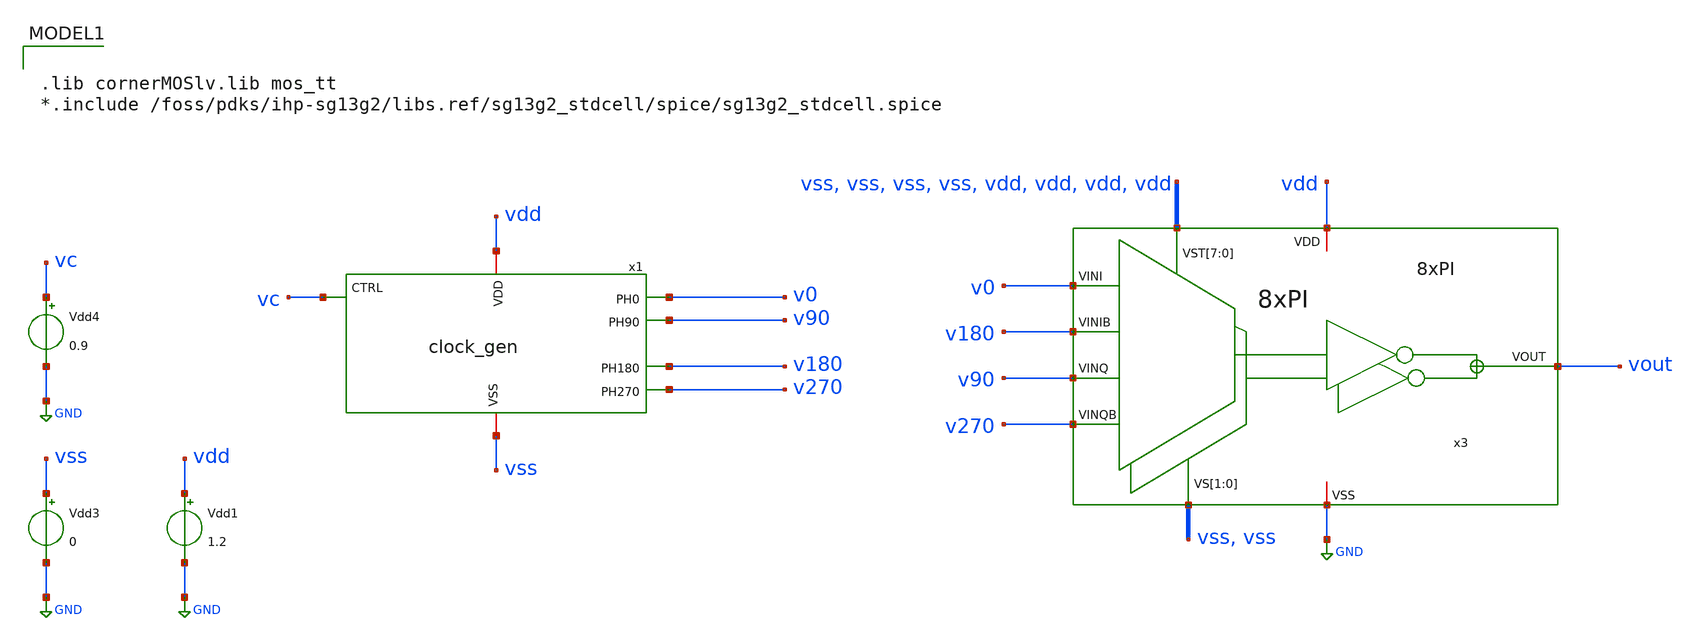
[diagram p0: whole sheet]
** sch_path: verification/testbenches/tb_Clock_Gen.sch
**.subckt tb_Clock_Gen
x1 v0 v90 vdd vc v180 vss v270 clock_gen
Vdd4 vc GND 0.9
Vdd3 vss GND 0
Vdd1 vdd GND 1.2
x3 v0 v180 v90 v270 vss vss vss vss vss vss vdd vdd vdd vdd vout vdd GND 8xPI
**** begin user architecture code

.lib cornerMOSlv.lib mos_tt
*.include /foss/pdks/ihp-sg13g2/libs.ref/sg13g2_stdcell/spice/sg13g2_stdcell.spice




.save v(v0) v(v1) v(v2) v(v3) v(v4) v(v5) v(v90) v(v270) v(v0_) v(v180) v(vout)

.tran 2p 5n

.control
run
set color0=white
write rosc.raw


*meas tran SKEW0_1 TRIG v(v0) VAL=0.6 RISE=3 TARG v(v1) VAL=0.6 RISE=4
*meas tran SKEW1_2 TRIG v(v1) VAL=0.6 RISE=3 TARG v(v2) VAL=0.6 RISE=4
*meas tran SKEW2_3 TRIG v(v2) VAL=0.6 RISE=3 TARG v(v3) VAL=0.6 RISE=4
*meas tran SKEW3_4 TRIG v(v3) VAL=0.6 RISE=3 TARG v(v4) VAL=0.6 RISE=5
*meas tran SKEW4_5 TRIG v(v4) VAL=0.6 RISE=3 TARG v(v5) VAL=0.6 RISE=4
*meas tran SKEW5_0 TRIG v(v5) VAL=0.6 RISE=3 TARG v(v0) VAL=0.6 RISE=4


*meas tran T0 TRIG v(v0) VAL=0.6 RISE=3 TARG v(v0) VAL=0.6 RISE=4
*meas tran T1 TRIG v(v1) VAL=0.6 RISE=3 TARG v(v1) VAL=0.6 RISE=4
*meas tran T2 TRIG v(v2) VAL=0.6 RISE=3 TARG v(v2) VAL=0.6 RISE=4
*meas tran T3 TRIG v(v3) VAL=0.6 RISE=3 TARG v(v3) VAL=0.6 RISE=4
*meas tran T4 TRIG v(v4) VAL=0.6 RISE=3 TARG v(v4) VAL=0.6 RISE=4
*meas tran T5 TRIG v(v5) VAL=0.6 RISE=3 TARG v(v5) VAL=0.6 RISE=4

*let period_0 = T0
*let period_1 = T1
*let period_2 = T2
*let period_3 = T3
*let period_4 = T4
*let period_5 = T5

*let phase0_1 = ((SKEW0_1 / period_0) * 360) -360
*let phase1_2 = ((SKEW1_2 / period_0) * 360) -360
*let phase2_3 = ((SKEW2_3 / period_0) * 360) -360
*let phase3_4 = ((SKEW3_4 / period_0) * 360) -360
*let phase4_5 = ((SKEW4_5 / period_0) * 360) -360
*let phase5_0 = ((SKEW5_0 / period_0) * 360) -360

*let freq0 = 1/T0
*let freq5 = 1/T5

*meas tran PW0 TRIG v(v0) VAL=0.6 RISE=3 TARG v(v0) VAL=0.6 FALL=4
*meas tran PW1 TRIG v(v1) VAL=0.6 RISE=3 TARG v(v1) VAL=0.6 FALL=4
*meas tran PW2 TRIG v(v2) VAL=0.6 RISE=3 TARG v(v2) VAL=0.6 FALL=4
*meas tran PW3 TRIG v(v3) VAL=0.6 RISE=3 TARG v(v3) VAL=0.6 FALL=4
*meas tran PW4 TRIG v(v4) VAL=0.6 RISE=3 TARG v(v4) VAL=0.6 FALL=4
*meas tran PW5 TRIG v(v5) VAL=0.6 RISE=3 TARG v(v5) VAL=0.6 FALL=4

*let Duty0 = PW0 / period_0
*let Duty1 = PW1 / period_1
*let Duty2 = PW2 / period_2
*let Duty3 = PW3 / period_3
*let Duty4 = PW4 / period_4
*let Duty5 = PW5 / period_5

meas tran SKEW0_90 TRIG v(v0) VAL=0.6 RISE=3 TARG v(v90) VAL=0.6 RISE=3
meas tran SKEW90_180 TRIG v(v90) VAL=0.6 RISE=3 TARG v(v180) VAL=0.6 RISE=4
meas tran SKEW180_270 TRIG v(v180) VAL=0.6 RISE=3 TARG v(v270) VAL=0.6 RISE=3
meas tran SKEW270_0 TRIG v(v270) VAL=0.6 RISE=3 TARG v(v0) VAL=0.6 RISE=3

meas tran T0 TRIG v(v0) VAL=0.6 RISE=3 TARG v(v0) VAL=0.6 RISE=4
meas tran T90 TRIG v(v90) VAL=0.6 RISE=3 TARG v(v90) VAL=0.6 RISE=4
meas tran T180 TRIG v(v180) VAL=0.6 RISE=3 TARG v(v180) VAL=0.6 RISE=4
meas tran T270 TRIG v(v270) VAL=0.6 RISE=3 TARG v(v270) VAL=0.6 RISE=4

let period_0 = T0
let period_90 = T90
let period_180 = T180
let period_270 = T270

let phase0_90 = ((SKEW0_90 / period_0) * 360)
let phase90_180 = ((SKEW90_180 / period_90) * 360)
let phase180_270 = ((SKEW180_270 / period_180) * 360)
let phase270_0 = ((SKEW270_0 / period_270) * 360)

meas tran PW0 TRIG v(v0) VAL=0.6 RISE=4 TARG v(v0) VAL=0.6 FALL=5
meas tran PW90 TRIG v(v90) VAL=0.6 RISE=3 TARG v(v90) VAL=0.6 FALL=4
meas tran PW180 TRIG v(v180) VAL=0.6 RISE=4 TARG v(v180) VAL=0.6 FALL=4
meas tran PW270 TRIG v(v270) VAL=0.6 RISE=4 TARG v(v270) VAL=0.6 FALL=4

let Duty0 = PW0 / period_0
let Duty90 = PW90 / period_90
let Duty180 = PW180 / period_180
let Duty270 = PW270 / period_270

let freq0 = 1/period_0

print phase0_90 phase90_180 phase180_270 phase270_0 Duty0 Duty90 Duty180 Duty270 freq0

.endc


**** end user architecture code
**.ends
.GLOBAL GND
.end
